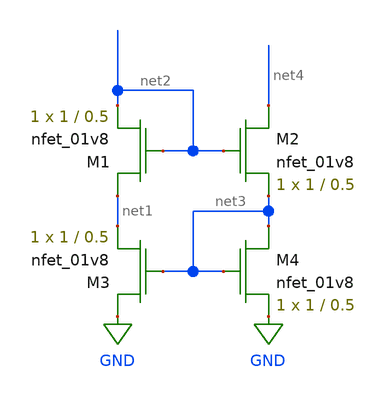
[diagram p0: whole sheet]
** sch_path: dac/schematics/misc/wilson_current_mirror.sch
**.subckt wilson_current_mirror
XM1 net1 net2 net2 GND sky130_fd_pr__nfet_01v8 L=0.5 W=1 nf=1 ad='int((nf+1)/2) * W/nf * 0.29' as='int((nf+2)/2) * W/nf * 0.29'
+ pd='2*int((nf+1)/2) * (W/nf + 0.29)' ps='2*int((nf+2)/2) * (W/nf + 0.29)' nrd='0.29 / W' nrs='0.29 / W'
+ sa=0 sb=0 sd=0 mult=1 m=1
XM2 net4 net2 net3 GND sky130_fd_pr__nfet_01v8 L=0.5 W=1 nf=1 ad='int((nf+1)/2) * W/nf * 0.29' as='int((nf+2)/2) * W/nf * 0.29'
+ pd='2*int((nf+1)/2) * (W/nf + 0.29)' ps='2*int((nf+2)/2) * (W/nf + 0.29)' nrd='0.29 / W' nrs='0.29 / W'
+ sa=0 sb=0 sd=0 mult=1 m=1
XM3 GND net3 net1 GND sky130_fd_pr__nfet_01v8 L=0.5 W=1 nf=1 ad='int((nf+1)/2) * W/nf * 0.29' as='int((nf+2)/2) * W/nf * 0.29'
+ pd='2*int((nf+1)/2) * (W/nf + 0.29)' ps='2*int((nf+2)/2) * (W/nf + 0.29)' nrd='0.29 / W' nrs='0.29 / W'
+ sa=0 sb=0 sd=0 mult=1 m=1
XM4 net3 net3 GND GND sky130_fd_pr__nfet_01v8 L=0.5 W=1 nf=1 ad='int((nf+1)/2) * W/nf * 0.29' as='int((nf+2)/2) * W/nf * 0.29'
+ pd='2*int((nf+1)/2) * (W/nf + 0.29)' ps='2*int((nf+2)/2) * (W/nf + 0.29)' nrd='0.29 / W' nrs='0.29 / W'
+ sa=0 sb=0 sd=0 mult=1 m=1
**.ends
.GLOBAL GND
.end
